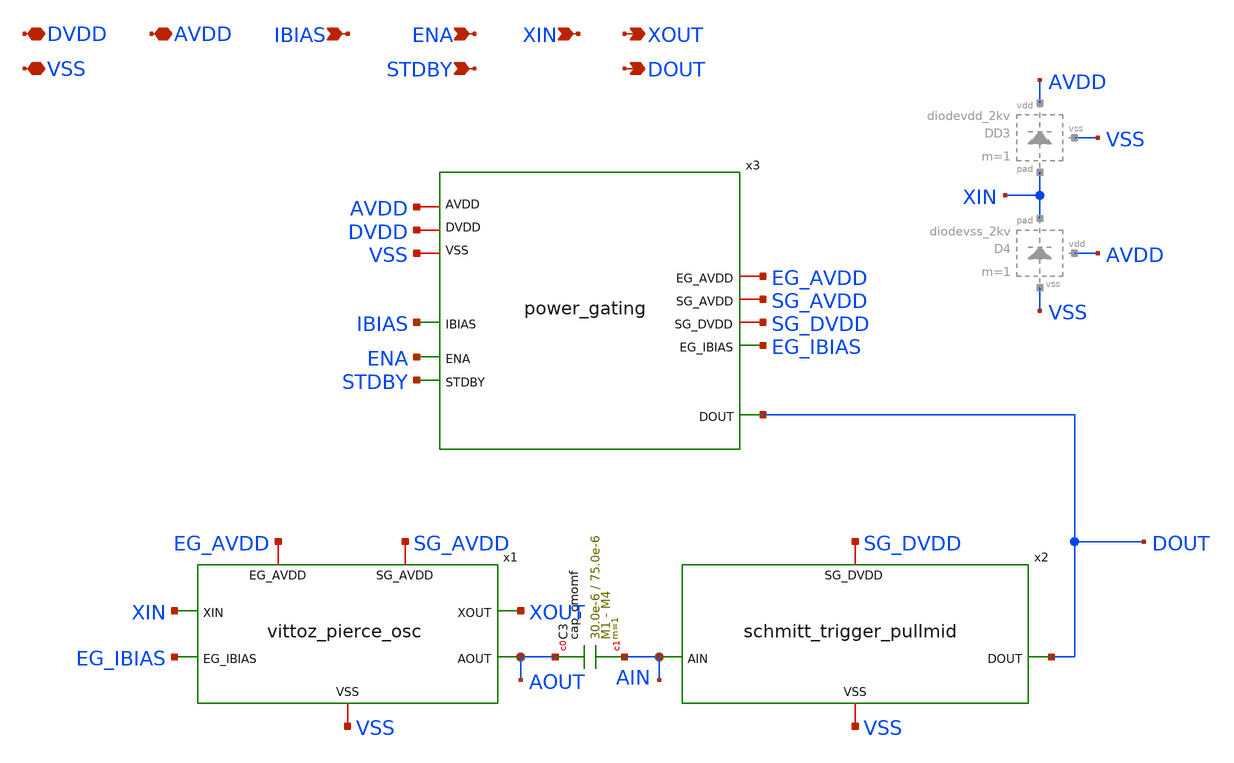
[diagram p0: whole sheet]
** sch_path: macros/sg13cmos5l_ht_ip__hsxo_cpz2/schematic/xschem/sg13cmos5l_ht_ip__hsxo_cpz2.sch
**.subckt sg13cmos5l_ht_ip__hsxo_cpz2 DVDD VSS AVDD ENA STDBY XIN XOUT DOUT IBIAS
*.iopin DVDD
*.iopin VSS
*.iopin AVDD
*.ipin ENA
*.ipin STDBY
*.ipin XIN
*.opin XOUT
*.opin DOUT
*.ipin IBIAS
x1 XOUT SG_AVDD EG_AVDD XIN EG_IBIAS AOUT VSS vittoz_pierce_osc
x2 SG_DVDD AIN DOUT VSS schmitt_trigger_pullmid
x3 DOUT SG_AVDD DVDD EG_IBIAS SG_DVDD AVDD IBIAS EG_AVDD ENA STDBY VSS power_gating
XC3 AOUT AIN cap_cmomf w=30.0e-6 l=75.0e-6 mmin=1 mmax=4 subblock=0 rfmodel=0 subscale=1 m=1 mm_ok=1
**.ends
.end
